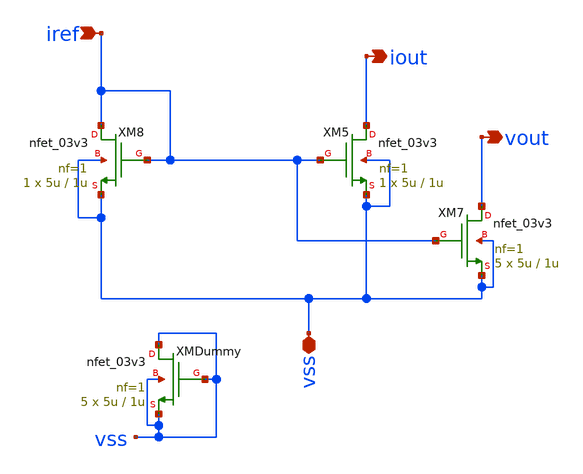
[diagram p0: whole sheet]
** sch_path: LDO/xschem/cm_nmos/symbol/cm_nmos.sch
**.subckt cm_nmos iref vss iout vout
*.ipin iref
*.iopin vss
*.opin iout
*.opin vout
XM5 iout iref vss vss nfet_03v3 L=1u W=5u nf=1 ad='int((nf+1)/2) * W/nf * 0.18u' as='int((nf+2)/2) * W/nf * 0.18u'
+ pd='2*int((nf+1)/2) * (W/nf + 0.18u)' ps='2*int((nf+2)/2) * (W/nf + 0.18u)' nrd='0.18u / W' nrs='0.18u / W'
+ sa=0 sb=0 sd=0 m=1
XM8 iref iref vss vss nfet_03v3 L=1u W=5u nf=1 ad='int((nf+1)/2) * W/nf * 0.18u' as='int((nf+2)/2) * W/nf * 0.18u'
+ pd='2*int((nf+1)/2) * (W/nf + 0.18u)' ps='2*int((nf+2)/2) * (W/nf + 0.18u)' nrd='0.18u / W' nrs='0.18u / W'
+ sa=0 sb=0 sd=0 m=1
XM7 vout iref vss vss nfet_03v3 L=1u W=5u nf=1 ad='int((nf+1)/2) * W/nf * 0.18u' as='int((nf+2)/2) * W/nf * 0.18u'
+ pd='2*int((nf+1)/2) * (W/nf + 0.18u)' ps='2*int((nf+2)/2) * (W/nf + 0.18u)' nrd='0.18u / W' nrs='0.18u / W'
+ sa=0 sb=0 sd=0 m=5
XMDummy vss vss vss vss nfet_03v3 L=1u W=5u nf=1 ad='int((nf+1)/2) * W/nf * 0.18u' as='int((nf+2)/2) * W/nf * 0.18u'
+ pd='2*int((nf+1)/2) * (W/nf + 0.18u)' ps='2*int((nf+2)/2) * (W/nf + 0.18u)' nrd='0.18u / W' nrs='0.18u / W'
+ sa=0 sb=0 sd=0 m=5
**.ends
.end
